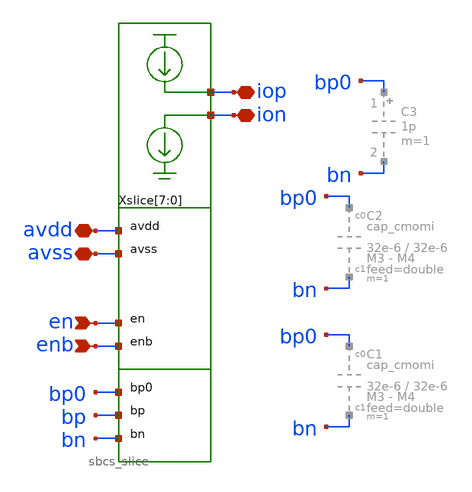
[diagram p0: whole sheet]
** sch_path: macros/sbcs/schematic/xschem/sbcs.sch
**.subckt sbcs avdd avss iop ion en enb
*.iopin avdd
*.iopin avss
*.iopin iop
*.iopin ion
*.ipin en
*.ipin enb
Xslice[7] iop ion avdd avss en enb bp0 bp bn sbcs_slice
Xslice[6] iop ion avdd avss en enb bp0 bp bn sbcs_slice
Xslice[5] iop ion avdd avss en enb bp0 bp bn sbcs_slice
Xslice[4] iop ion avdd avss en enb bp0 bp bn sbcs_slice
Xslice[3] iop ion avdd avss en enb bp0 bp bn sbcs_slice
Xslice[2] iop ion avdd avss en enb bp0 bp bn sbcs_slice
Xslice[1] iop ion avdd avss en enb bp0 bp bn sbcs_slice
Xslice[0] iop ion avdd avss en enb bp0 bp bn sbcs_slice
**.ends
.end
